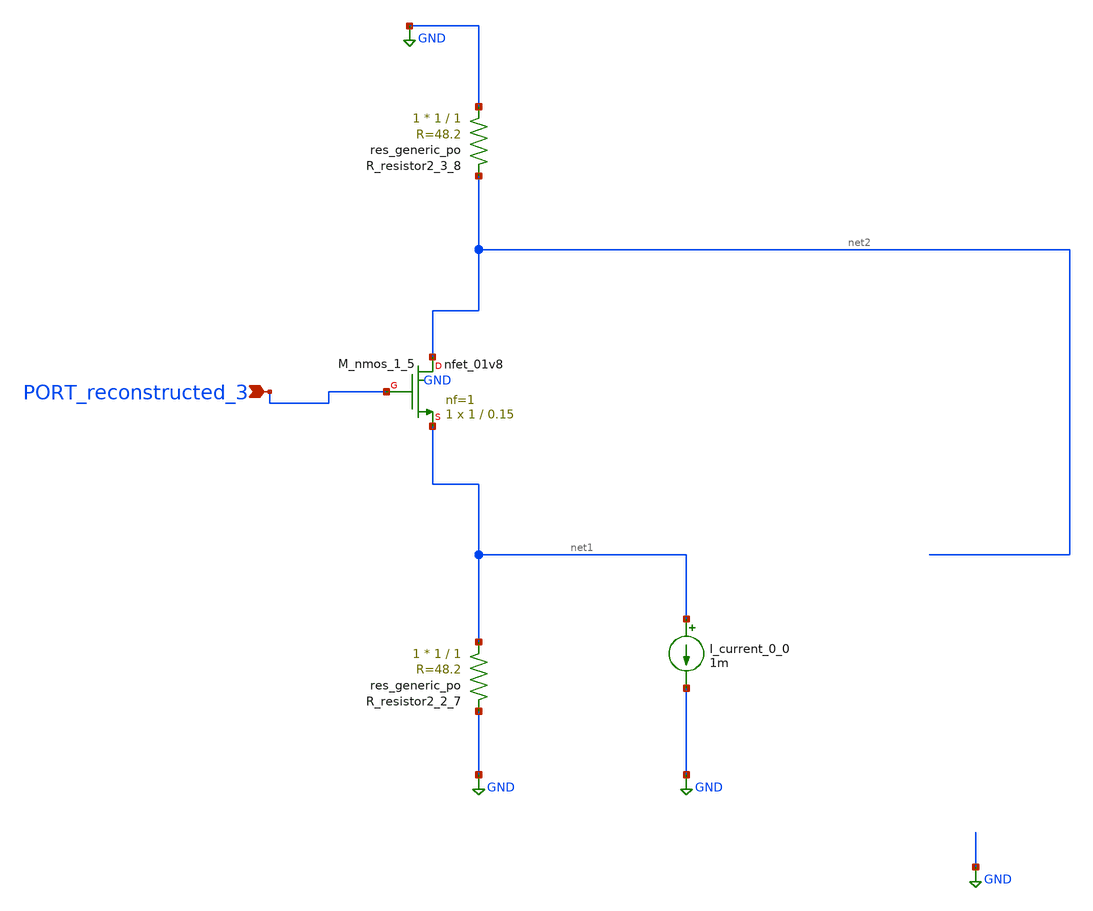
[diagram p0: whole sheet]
** sch_path: schematics/AMSNet/678.sch
**.subckt 678 PORT_reconstructed_3
*.ipin PORT_reconstructed_3
I_current_0_0 net1 GND 1m
XM_nmos_1_5 net2 PORT_reconstructed_3 net1 GND sky130_fd_pr__nfet_01v8 L=0.15 W=1 nf=1 ad='int((1 + 1)/2) * 1 / 1 * 0.29'
+ as='int((1 + 2)/2) * 1 / 1 * 0.29' pd='2*int((1 + 1)/2) * (1 / 1 + 0.29)' ps='2*int((1 + 2)/2) * (1 / 1 + 0.29)'
+ nrd='0.29 / 1 ' nrs='0.29 / 1 ' sa=0 sb=0 sd=0 mult=1 m=1
XR_resistor2_2_7 net1 GND sky130_fd_pr__res_generic_po W=1 L=1 m=1
XR_resistor2_3_8 GND net2 sky130_fd_pr__res_generic_po W=1 L=1 m=1
**.ends
.GLOBAL GND
.end
